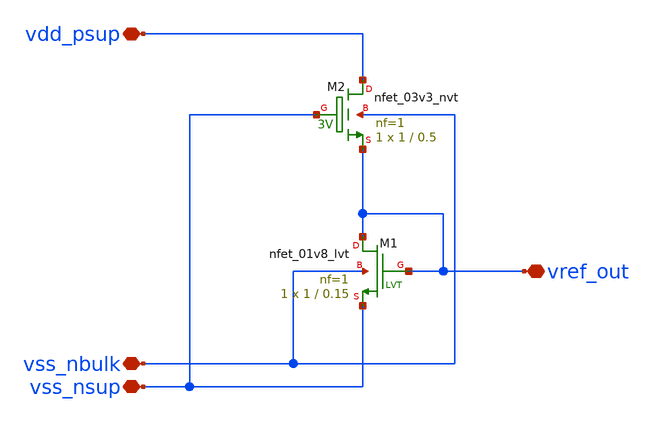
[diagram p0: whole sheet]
** sch_path: xschem/test_schematic_1.sch
**.subckt test_schematic_1 vdd_psup vss_nbulk vss_nsup vref_out
*.iopin vdd_psup
*.iopin vss_nbulk
*.iopin vss_nsup
*.iopin vref_out
XM1 vref_out vref_out vss_nsup vss_nbulk sky130_fd_pr__nfet_01v8_lvt L=0.15 W=1 nf=1 ad='int((nf+1)/2) * W/nf * 0.29'
+ as='int((nf+2)/2) * W/nf * 0.29' pd='2*int((nf+1)/2) * (W/nf + 0.29)' ps='2*int((nf+2)/2) * (W/nf + 0.29)'
+ nrd='0.29 / W' nrs='0.29 / W' sa=0 sb=0 sd=0 mult=1 m=1
XM2 vdd_psup vss_nsup vref_out vss_nbulk sky130_fd_pr__nfet_03v3_nvt L=0.5 W=1 nf=1 ad='int((nf+1)/2) * W/nf * 0.29'
+ as='int((nf+2)/2) * W/nf * 0.29' pd='2*int((nf+1)/2) * (W/nf + 0.29)' ps='2*int((nf+2)/2) * (W/nf + 0.29)'
+ nrd='0.29 / W' nrs='0.29 / W' sa=0 sb=0 sd=0 mult=1 m=1
**.ends
.end
